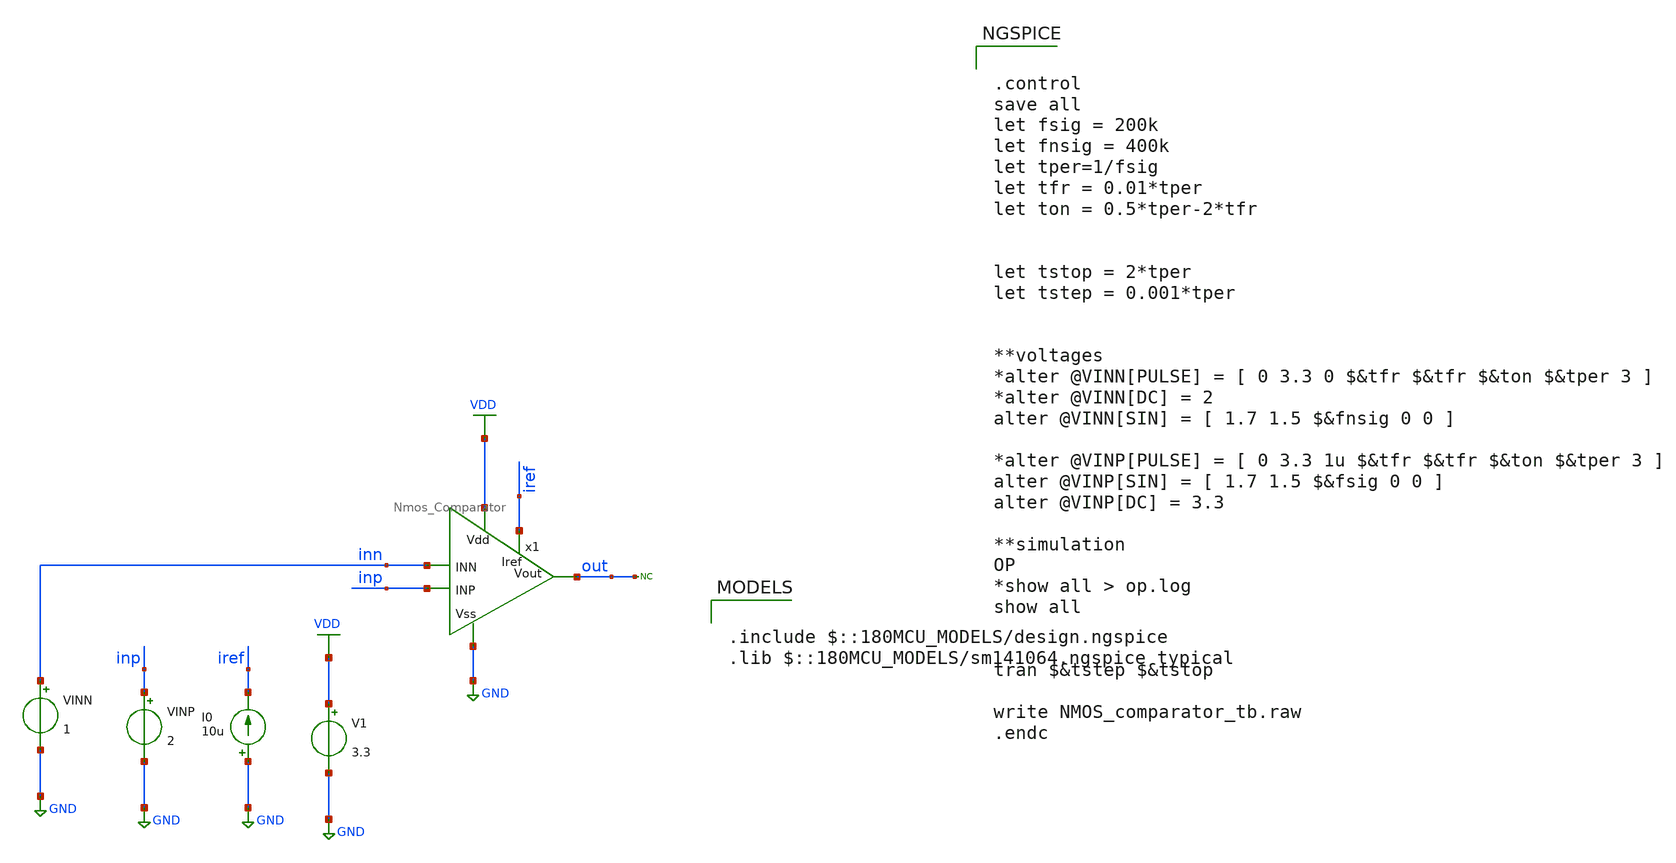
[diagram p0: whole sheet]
** sch_path: designs/libs/tb_analog/Comparator/NMOS_comparator_tb.sch
**.subckt NMOS_comparator_tb
I0 GND iref 10u
V1 VDD GND 3.3
VINP inp GND 2
* noconn out
VINN inn GND 1
x1 VDD out inn inp iref GND Nmos_Comparator
**** begin user architecture code


.control
save all
let fsig = 200k
let fnsig = 400k
let tper=1/fsig
let tfr = 0.01*tper
let ton = 0.5*tper-2*tfr


let tstop = 2*tper
let tstep = 0.001*tper


**voltages
*alter @VINN[PULSE] = [ 0 3.3 0 $&tfr $&tfr $&ton $&tper 3 ]
*alter @VINN[DC] = 2
alter @VINN[SIN] = [ 1.7 1.5 $&fnsig 0 0 ]

*alter @VINP[PULSE] = [ 0 3.3 1u $&tfr $&tfr $&ton $&tper 3 ]
alter @VINP[SIN] = [ 1.7 1.5 $&fsig 0 0 ]
alter @VINP[DC] = 3.3

**simulation
OP
*show all > op.log
show all


tran $&tstep $&tstop

write NMOS_comparator_tb.raw
.endc



.include $::180MCU_MODELS/design.ngspice
.lib $::180MCU_MODELS/sm141064.ngspice typical

**** end user architecture code
**.ends

* expanding   symbol:  libs/core_analog/Comparator/Nmos_Comparator.sym # of pins=6
** sym_path: designs/libs/core_analog/Comparator/Nmos_Comparator.sym
** sch_path: designs/libs/core_analog/Comparator/Nmos_Comparator.sch
.subckt Nmos_Comparator Vdd Vout INN INP Iref Vss
*.ipin vss
*.ipin vdd
*.ipin iref
*.ipin inn
*.ipin inp
*.opin vout
XM3 net1 net1 vss vss nfet_03v3 L=1u W=3.5u nf=1 ad='int((nf+1)/2) * W/nf * 0.18u' as='int((nf+2)/2) * W/nf * 0.18u'
+ pd='2*int((nf+1)/2) * (W/nf + 0.18u)' ps='2*int((nf+2)/2) * (W/nf + 0.18u)' nrd='0.18u / W' nrs='0.18u / W'
+ sa=0 sb=0 sd=0 m=1
XM4 vout net1 vss vss nfet_03v3 L=1u W=3.5u nf=1 ad='int((nf+1)/2) * W/nf * 0.18u' as='int((nf+2)/2) * W/nf * 0.18u'
+ pd='2*int((nf+1)/2) * (W/nf + 0.18u)' ps='2*int((nf+2)/2) * (W/nf + 0.18u)' nrd='0.18u / W' nrs='0.18u / W'
+ sa=0 sb=0 sd=0 m=1
XM5 net2 inn net3 vss nfet_03v3 L=1u W=4u nf=1 ad='int((nf+1)/2) * W/nf * 0.18u' as='int((nf+2)/2) * W/nf * 0.18u'
+ pd='2*int((nf+1)/2) * (W/nf + 0.18u)' ps='2*int((nf+2)/2) * (W/nf + 0.18u)' nrd='0.18u / W' nrs='0.18u / W'
+ sa=0 sb=0 sd=0 m=1
XM6 net4 inp net3 vss nfet_03v3 L=1u W=4u nf=1 ad='int((nf+1)/2) * W/nf * 0.18u' as='int((nf+2)/2) * W/nf * 0.18u'
+ pd='2*int((nf+1)/2) * (W/nf + 0.18u)' ps='2*int((nf+2)/2) * (W/nf + 0.18u)' nrd='0.18u / W' nrs='0.18u / W'
+ sa=0 sb=0 sd=0 m=1
XM7 net1 net2 vdd vdd pfet_03v3 L=0.5u W=16.5u nf=4 ad='int((nf+1)/2) * W/nf * 0.18u' as='int((nf+2)/2) * W/nf * 0.18u'
+ pd='2*int((nf+1)/2) * (W/nf + 0.18u)' ps='2*int((nf+2)/2) * (W/nf + 0.18u)' nrd='0.18u / W' nrs='0.18u / W'
+ sa=0 sb=0 sd=0 m=1
XM9 net4 net4 vdd vdd pfet_03v3 L=0.5u W=10u nf=2 ad='int((nf+1)/2) * W/nf * 0.18u' as='int((nf+2)/2) * W/nf * 0.18u'
+ pd='2*int((nf+1)/2) * (W/nf + 0.18u)' ps='2*int((nf+2)/2) * (W/nf + 0.18u)' nrd='0.18u / W' nrs='0.18u / W'
+ sa=0 sb=0 sd=0 m=1
XM11 net2 net2 vdd vdd pfet_03v3 L=0.5u W=10u nf=2 ad='int((nf+1)/2) * W/nf * 0.18u' as='int((nf+2)/2) * W/nf * 0.18u'
+ pd='2*int((nf+1)/2) * (W/nf + 0.18u)' ps='2*int((nf+2)/2) * (W/nf + 0.18u)' nrd='0.18u / W' nrs='0.18u / W'
+ sa=0 sb=0 sd=0 m=1
XM12 vout net4 vdd vdd pfet_03v3 L=0.5u W=16.5u nf=4 ad='int((nf+1)/2) * W/nf * 0.18u' as='int((nf+2)/2) * W/nf * 0.18u'
+ pd='2*int((nf+1)/2) * (W/nf + 0.18u)' ps='2*int((nf+2)/2) * (W/nf + 0.18u)' nrd='0.18u / W' nrs='0.18u / W'
+ sa=0 sb=0 sd=0 m=1
XM1 net4 net2 vdd vdd pfet_03v3 L=0.5u W=10u nf=2 ad='int((nf+1)/2) * W/nf * 0.18u' as='int((nf+2)/2) * W/nf * 0.18u'
+ pd='2*int((nf+1)/2) * (W/nf + 0.18u)' ps='2*int((nf+2)/2) * (W/nf + 0.18u)' nrd='0.18u / W' nrs='0.18u / W'
+ sa=0 sb=0 sd=0 m=1
XM2 net2 net4 vdd vdd pfet_03v3 L=0.5u W=10u nf=2 ad='int((nf+1)/2) * W/nf * 0.18u' as='int((nf+2)/2) * W/nf * 0.18u'
+ pd='2*int((nf+1)/2) * (W/nf + 0.18u)' ps='2*int((nf+2)/2) * (W/nf + 0.18u)' nrd='0.18u / W' nrs='0.18u / W'
+ sa=0 sb=0 sd=0 m=1
XM8 iref iref vss vss nfet_03v3 L=1u W=2.5u nf=1 ad='int((nf+1)/2) * W/nf * 0.18u' as='int((nf+2)/2) * W/nf * 0.18u'
+ pd='2*int((nf+1)/2) * (W/nf + 0.18u)' ps='2*int((nf+2)/2) * (W/nf + 0.18u)' nrd='0.18u / W' nrs='0.18u / W'
+ sa=0 sb=0 sd=0 m=1
XM10 net3 iref vss vss nfet_03v3 L=1u W=5u nf=2 ad='int((nf+1)/2) * W/nf * 0.18u' as='int((nf+2)/2) * W/nf * 0.18u'
+ pd='2*int((nf+1)/2) * (W/nf + 0.18u)' ps='2*int((nf+2)/2) * (W/nf + 0.18u)' nrd='0.18u / W' nrs='0.18u / W'
+ sa=0 sb=0 sd=0 m=1
.ends

.GLOBAL GND
.GLOBAL VDD
.end
